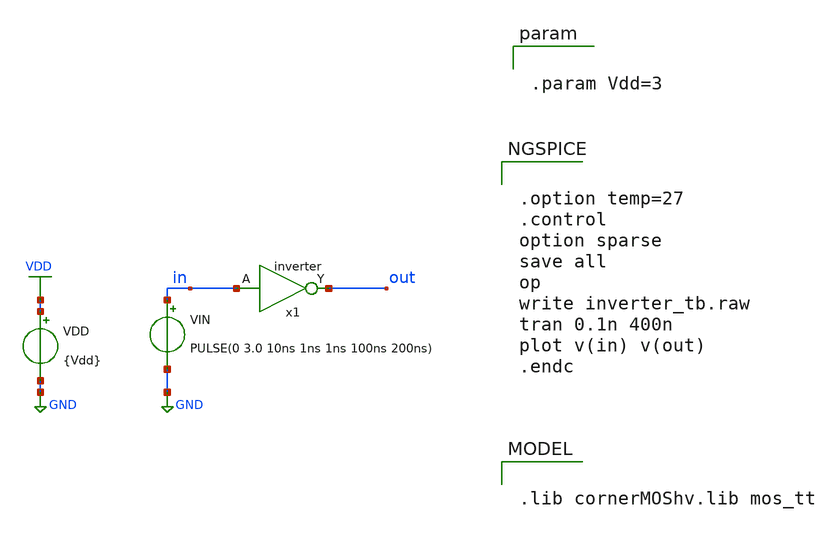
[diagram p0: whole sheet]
** sch_path: 3_real_circuits/inverter_tb.sch
**.subckt inverter_tb
x1 in out inverter
VDD VDD GND {Vdd}
VIN in GND PULSE(0 3.0 10ns 1ns 1ns 100ns 200ns)
**** begin user architecture code


.param Vdd=3




.option temp=27
.control
option sparse
save all
op
write inverter_tb.raw
tran 0.1n 400n
plot v(in) v(out)
.endc



.lib cornerMOShv.lib mos_tt

**** end user architecture code
**.ends

* expanding   symbol:  inverter.sym # of pins=2
** sym_path: 3_real_circuits/inverter.sym
** sch_path: 3_real_circuits/inverter.sch
.subckt inverter A Y
*.opin Y
*.ipin A
XM2 Y A GND GND sg13_hv_nmos w=0.3u l=0.45u ng=1 m=1 mm_ok=1
XM1 Y A VDD VDD sg13_hv_pmos w=0.3u l=0.4u ng=1 m=1 mm_ok=1
.ends

.GLOBAL VDD
.GLOBAL GND
.end
